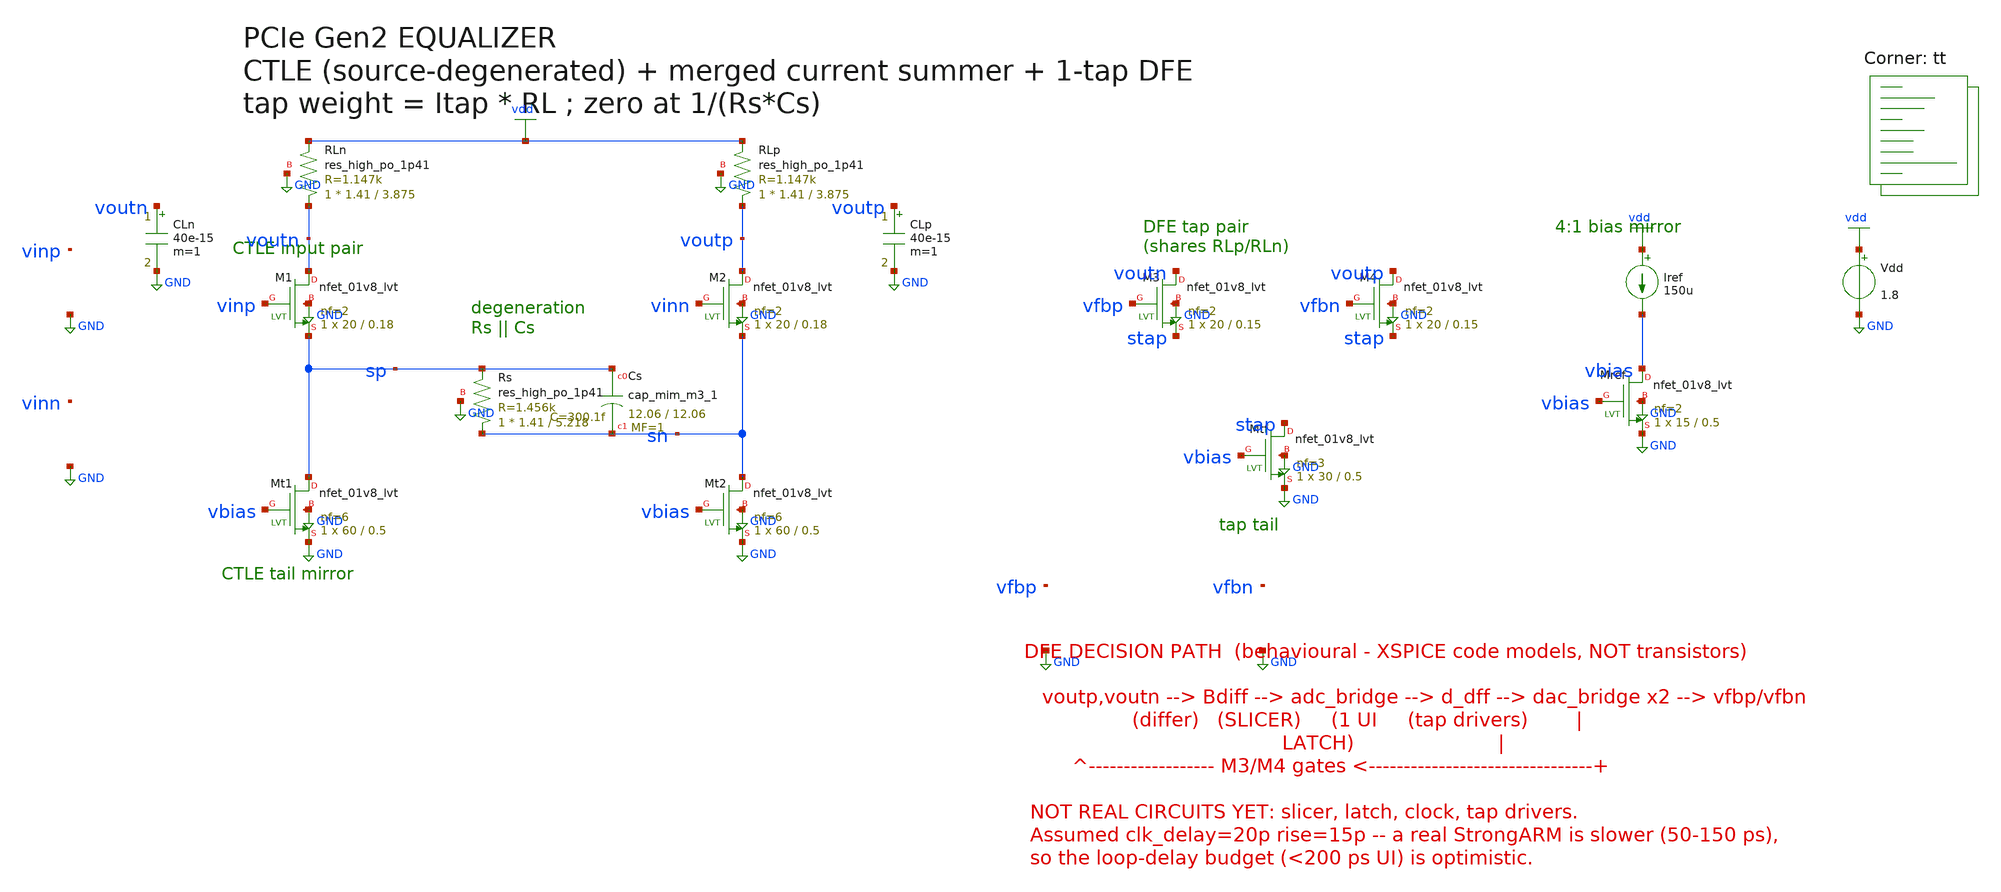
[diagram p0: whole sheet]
** sch_path: netlists/eq_dfe_tb.sch
**.subckt eq_dfe_tb
XM1 voutn vinp sp GND sky130_fd_pr__nfet_01v8_lvt L=0.18 W=20 nf=2 ad=0 as=0 pd=0 ps=0 nrd=0 nrs=0
+ sa=0 sb=0 sd=0 mult=1 m=1
XM2 voutp vinn sn GND sky130_fd_pr__nfet_01v8_lvt L=0.18 W=20 nf=2 ad=0 as=0 pd=0 ps=0 nrd=0 nrs=0
+ sa=0 sb=0 sd=0 mult=1 m=1
XRLn voutn vdd GND sky130_fd_pr__res_high_po_1p41 L=3.875 mult=1 m=1
XRLp voutp vdd GND sky130_fd_pr__res_high_po_1p41 L=3.875 mult=1 m=1
XRs sn sp GND sky130_fd_pr__res_high_po_1p41 L=5.218 mult=1 m=1
XCs sp sn sky130_fd_pr__cap_mim_m3_1 W=12.06 L=12.06 MF=1 m=1
CLn voutn GND 40e-15 m=1
CLp voutp GND 40e-15 m=1
XMt1 sp vbias GND GND sky130_fd_pr__nfet_01v8_lvt L=0.5 W=60 nf=6 ad=0 as=0 pd=0 ps=0 nrd=0 nrs=0
+ sa=0 sb=0 sd=0 mult=1 m=1
XMt2 sn vbias GND GND sky130_fd_pr__nfet_01v8_lvt L=0.5 W=60 nf=6 ad=0 as=0 pd=0 ps=0 nrd=0 nrs=0
+ sa=0 sb=0 sd=0 mult=1 m=1
XM3 voutn vfbp stap GND sky130_fd_pr__nfet_01v8_lvt L=0.15 W=20 nf=2 ad=0 as=0 pd=0 ps=0 nrd=0 nrs=0
+ sa=0 sb=0 sd=0 mult=1 m=1
XM4 voutp vfbn stap GND sky130_fd_pr__nfet_01v8_lvt L=0.15 W=20 nf=2 ad=0 as=0 pd=0 ps=0 nrd=0 nrs=0
+ sa=0 sb=0 sd=0 mult=1 m=1
XMtf stap vbias GND GND sky130_fd_pr__nfet_01v8_lvt L=0.5 W=30 nf=3 ad=0 as=0 pd=0 ps=0 nrd=0 nrs=0
+ sa=0 sb=0 sd=0 mult=1 m=1
XMref vbias vbias GND GND sky130_fd_pr__nfet_01v8_lvt L=0.5 W=15 nf=2 ad=0 as=0 pd=0 ps=0 nrd=0
+ nrs=0 sa=0 sb=0 sd=0 mult=1 m=1
Iref vdd vbias 150u
Vdd vdd GND 1.8
**** begin user architecture code
.lib $::SKYWATER_MODELS/sky130.lib.spice tt
**** end user architecture code
**.ends
.GLOBAL vdd
.GLOBAL GND
**** begin user architecture code


* ---- PRBS-7 NRZ stimulus, 5 Gb/s, 100 mV differential ----
Vinp vinp 0 PWL(0 1.15 1.85e-10 1.15 2.15e-10 1.05 3.85e-10 1.05 4.15e-10 1.15 9.85e-10 1.15
+ 1.015e-09 1.05 1.385e-09 1.05 1.415e-09 1.15 1.785e-09 1.15 1.815e-09 1.05 2.185e-09 1.05 2.215e-09 1.15
+ 2.385e-09 1.15 2.415e-09 1.05 2.585e-09 1.05 2.615e-09 1.15 2.785e-09 1.15 2.815e-09 1.05 2.985e-09 1.05
+ 3.015e-09 1.15 3.185e-09 1.15 3.215e-09 1.05 3.385e-09 1.05 3.415e-09 1.15 4.785e-09 1.15 4.815e-09 1.05
+ 5.985e-09 1.05 6.015e-09 1.15 6.185e-09 1.15 6.215e-09 1.05 7.185e-09 1.05 7.215e-09 1.15 7.585e-09 1.15
+ 7.615e-09 1.05 8.385e-09 1.05 8.415e-09 1.15 8.585e-09 1.15 8.615e-09 1.05 8.785e-09 1.05 8.815e-09 1.15
+ 8.985e-09 1.15 9.015e-09 1.05 9.585e-09 1.05 9.615e-09 1.15 1.0385e-08 1.15 1.0415e-08 1.05 1.0785e-08 1.05
+ 1.0815e-08 1.15 1.0985e-08 1.15 1.1015e-08 1.05 1.1585e-08 1.05 1.1615e-08 1.15 1.1785e-08 1.15 1.1815e-08
+ 1.05 1.1985e-08 1.05 1.2015e-08 1.15 1.2385e-08 1.15 1.2415e-08 1.05 1.28e-08 1.05)
Vinn vinn 0 PWL(0 1.05 1.85e-10 1.05 2.15e-10 1.15 3.85e-10 1.15 4.15e-10 1.05 9.85e-10 1.05
+ 1.015e-09 1.15 1.385e-09 1.15 1.415e-09 1.05 1.785e-09 1.05 1.815e-09 1.15 2.185e-09 1.15 2.215e-09 1.05
+ 2.385e-09 1.05 2.415e-09 1.15 2.585e-09 1.15 2.615e-09 1.05 2.785e-09 1.05 2.815e-09 1.15 2.985e-09 1.15
+ 3.015e-09 1.05 3.185e-09 1.05 3.215e-09 1.15 3.385e-09 1.15 3.415e-09 1.05 4.785e-09 1.05 4.815e-09 1.15
+ 5.985e-09 1.15 6.015e-09 1.05 6.185e-09 1.05 6.215e-09 1.15 7.185e-09 1.15 7.215e-09 1.05 7.585e-09 1.05
+ 7.615e-09 1.15 8.385e-09 1.15 8.415e-09 1.05 8.585e-09 1.05 8.615e-09 1.15 8.785e-09 1.15 8.815e-09 1.05
+ 8.985e-09 1.05 9.015e-09 1.15 9.585e-09 1.15 9.615e-09 1.05 1.0385e-08 1.05 1.0415e-08 1.15 1.0785e-08 1.15
+ 1.0815e-08 1.05 1.0985e-08 1.05 1.1015e-08 1.15 1.1585e-08 1.15 1.1615e-08 1.05 1.1785e-08 1.05 1.1815e-08
+ 1.15 1.1985e-08 1.15 1.2015e-08 1.05 1.2385e-08 1.05 1.2415e-08 1.15 1.28e-08 1.15)
* ---- DFE decision path ----
Bdiff vdiff 0 V=V(voutp)-V(voutn)
Vclk clk 0 DC 0 PULSE(0 1.8 1e-10 10p 10p 8e-11 2e-10)
adc_in  [vdiff] [ddata] adc_sl
adc_clk [clk]   [dclk]  adc_ck
aff ddata dclk NULL NULL dq dqb dff_1tap
* POLARITY: dqb (NOT dq) drives vfbp. X3's drain is voutn, so vfbp high pulls
* voutn down and drives (voutp-voutn) POSITIVE. Feeding the previous decision
* dq straight to vfbp therefore REINFORCES that bit -- the opposite of what a
* DFE must do. The tap has to SUBTRACT the post-cursor, so the inverted output
* drives vfbp. Measured at Itap=150uA: dq->vfbp gives 0.078 UI, dqb->vfbp gives
* 0.453 UI.
adac_p [dqb] [vfbp] dac_fb
adac_n [dq]  [vfbn] dac_fb
.model adc_sl  adc_bridge(in_low=-0.001 in_high=0.001)
.model adc_ck  adc_bridge(in_low=0.7 in_high=1.1)
.model dac_fb  dac_bridge(out_low=0.8 out_high=1.4 out_undef=1.1 t_rise=15p t_fall=15p)
.model dff_1tap d_dff(clk_delay=20p rise_delay=15p fall_delay=15p)
.control
tran 4p 1.28e-08 0 4p
let vd = v(voutp)-v(voutn)
echo ---------- closed-loop DFE: eye should be OPEN ----------
plot vd
plot v(vfbp) v(vfbn)
.endc


**** end user architecture code
.end
